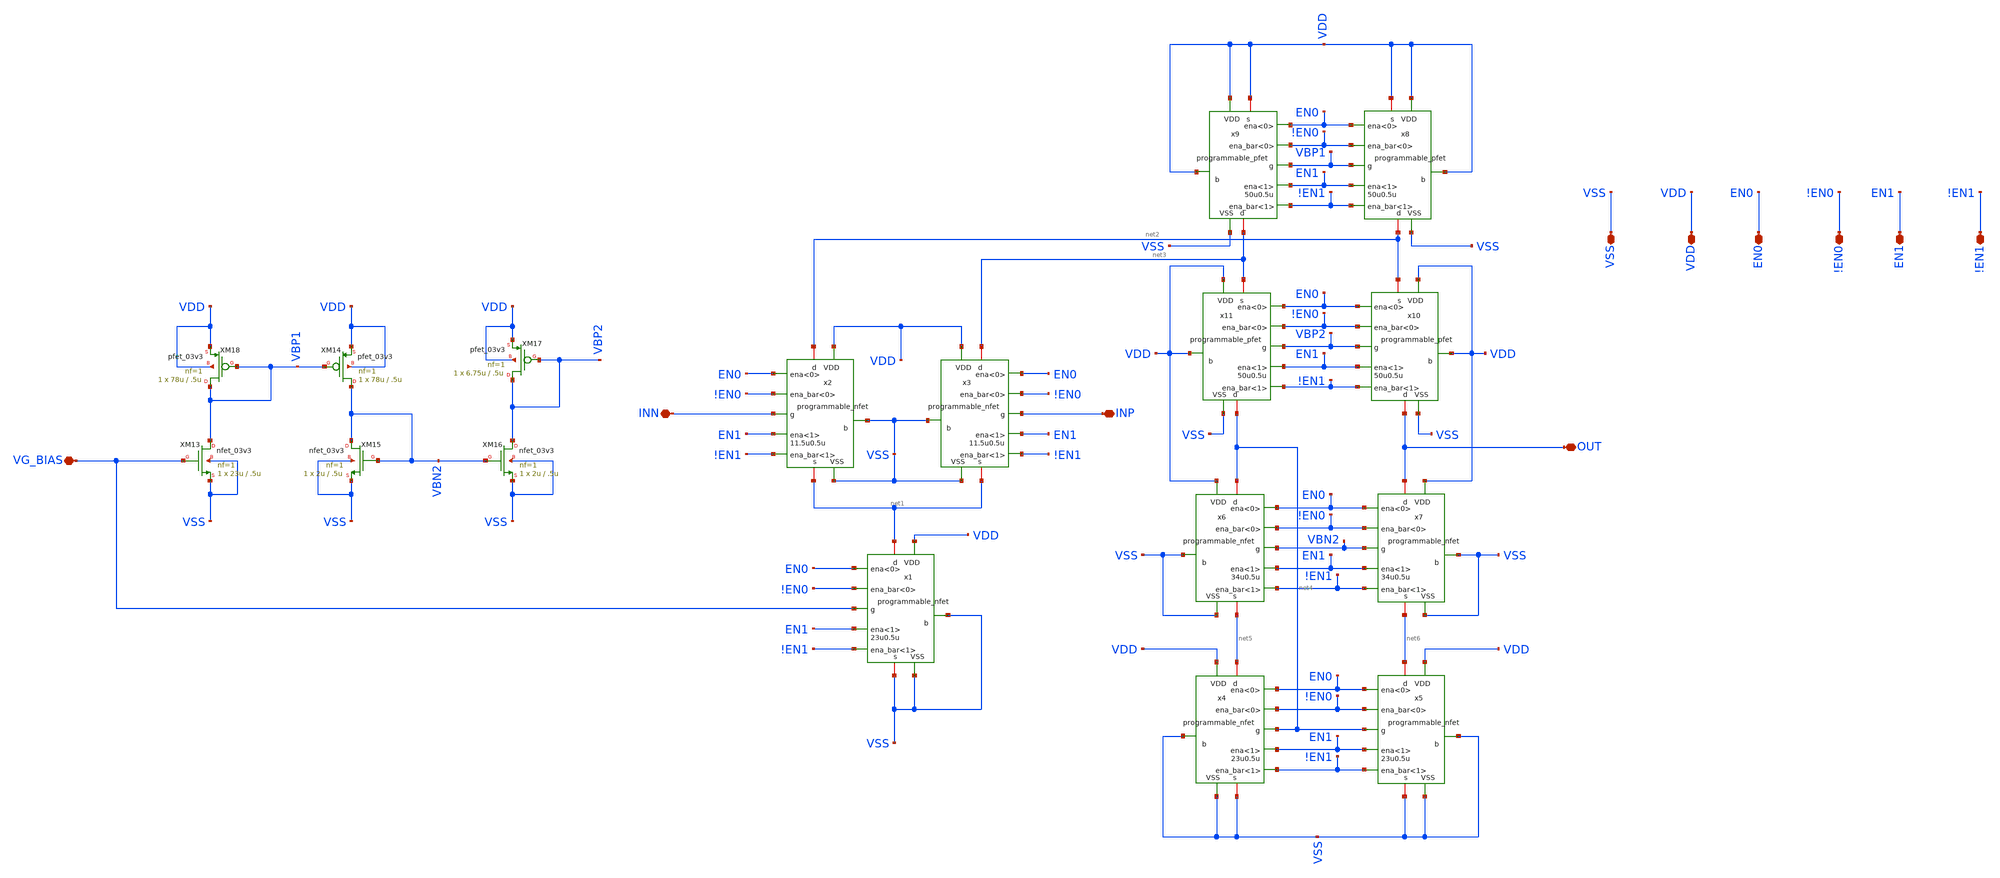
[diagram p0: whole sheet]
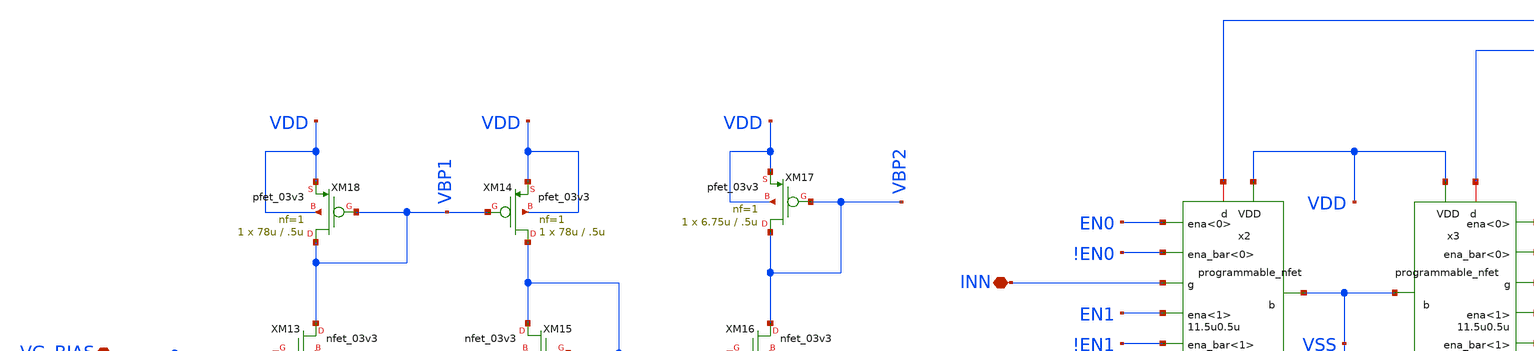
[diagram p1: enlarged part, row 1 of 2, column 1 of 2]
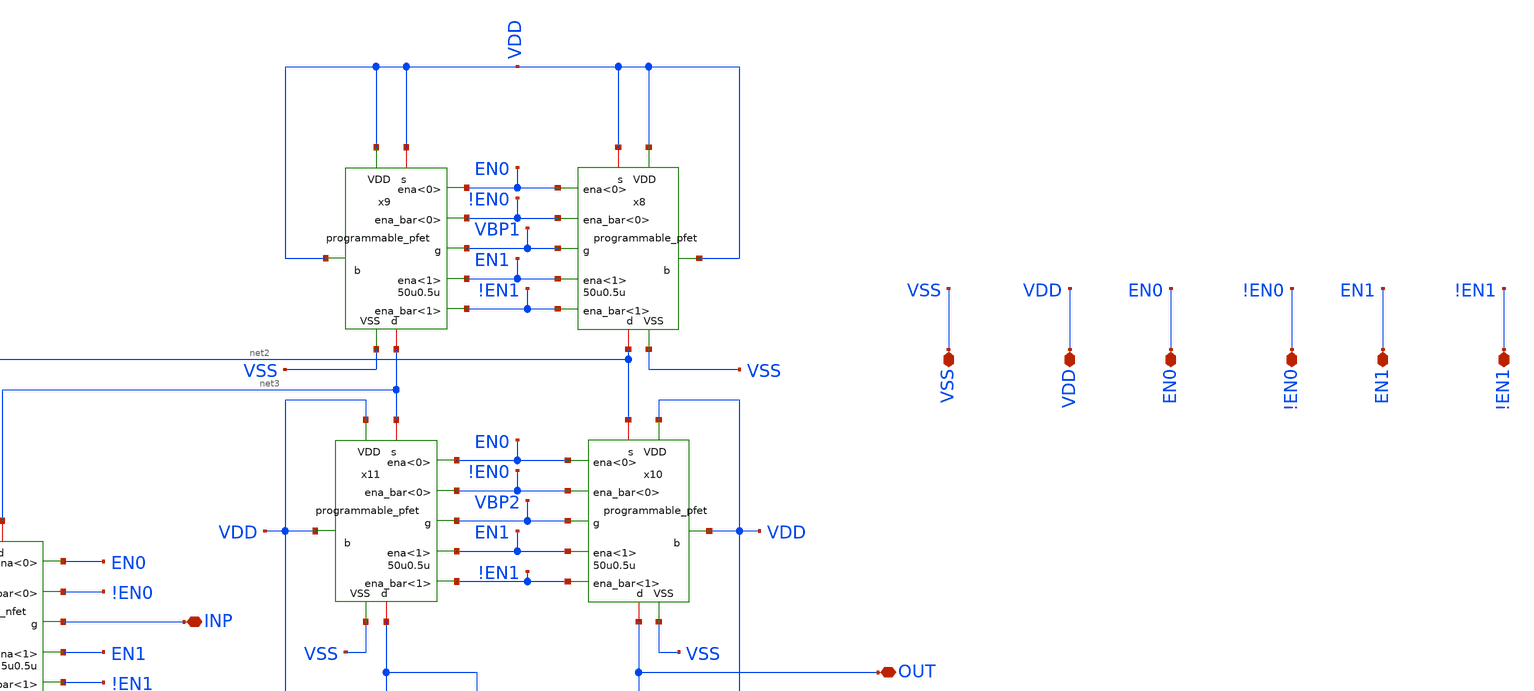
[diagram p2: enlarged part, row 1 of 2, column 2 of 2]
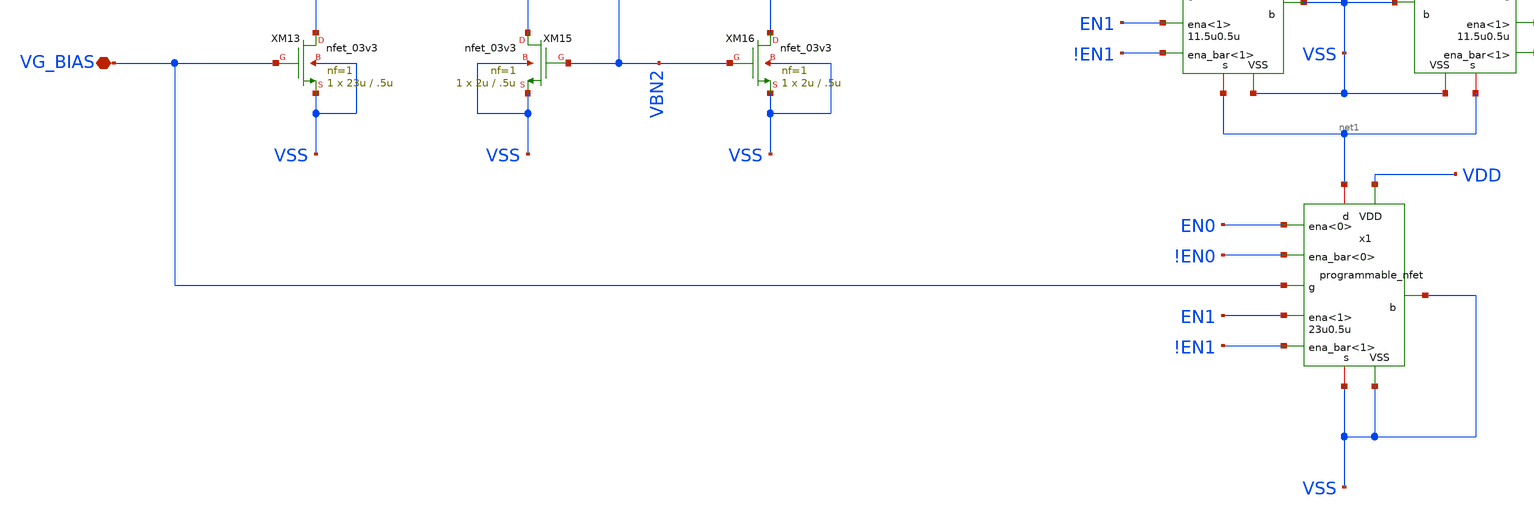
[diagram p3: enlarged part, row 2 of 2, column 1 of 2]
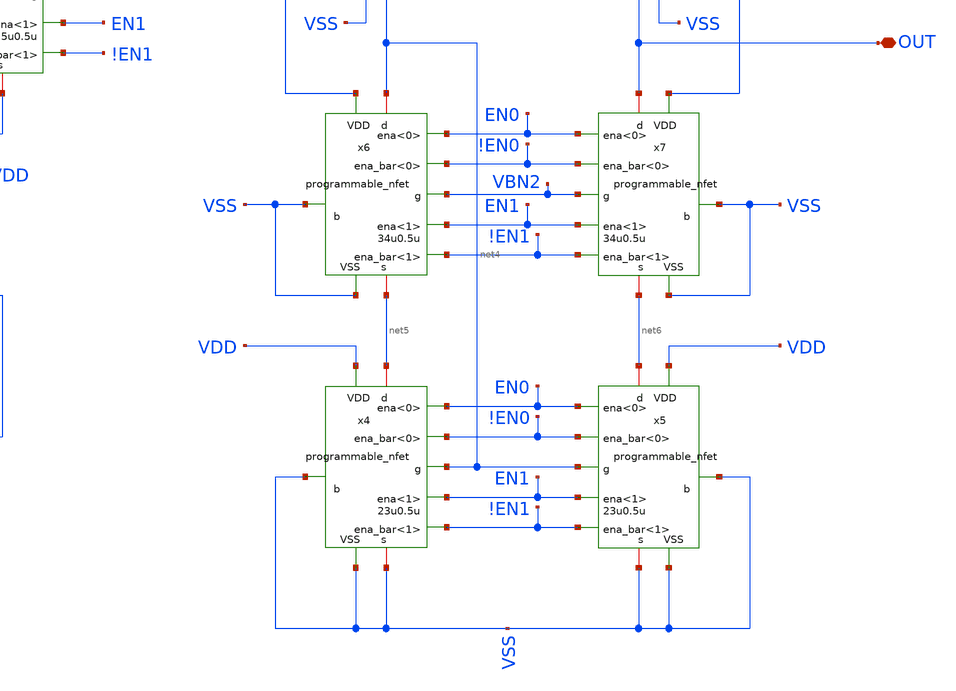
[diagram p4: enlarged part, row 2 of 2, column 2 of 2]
** sch_path: designs/libs/old_amps/ota_folded_cascode/programmable_folded.sch
**.subckt programmable_folded OUT VSS VDD EN0 !EN0 EN1 !EN1 INN INP VG_BIAS
*.iopin OUT
*.iopin VSS
*.iopin VDD
*.iopin EN0
*.iopin !EN0
*.iopin EN1
*.iopin !EN1
*.iopin INN
*.iopin INP
*.iopin VG_BIAS
XM18 VBP1 VBP1 VDD VDD pfet_03v3 L=.5u W=78u nf=1 ad='int((nf+1)/2) * W/nf * 0.18u' as='int((nf+2)/2) * W/nf * 0.18u'
+ pd='2*int((nf+1)/2) * (W/nf + 0.18u)' ps='2*int((nf+2)/2) * (W/nf + 0.18u)' nrd='0.18u / W' nrs='0.18u / W'
+ sa=0 sb=0 sd=0 m=1
XM13 VBP1 VG_BIAS VSS VSS nfet_03v3 L=.5u W=23u nf=1 ad='int((nf+1)/2) * W/nf * 0.18u' as='int((nf+2)/2) * W/nf * 0.18u'
+ pd='2*int((nf+1)/2) * (W/nf + 0.18u)' ps='2*int((nf+2)/2) * (W/nf + 0.18u)' nrd='0.18u / W' nrs='0.18u / W'
+ sa=0 sb=0 sd=0 m=1
XM14 VBN2 VBP1 VDD VDD pfet_03v3 L=.5u W=78u nf=1 ad='int((nf+1)/2) * W/nf * 0.18u' as='int((nf+2)/2) * W/nf * 0.18u'
+ pd='2*int((nf+1)/2) * (W/nf + 0.18u)' ps='2*int((nf+2)/2) * (W/nf + 0.18u)' nrd='0.18u / W' nrs='0.18u / W'
+ sa=0 sb=0 sd=0 m=1
XM15 VBN2 VBN2 VSS VSS nfet_03v3 L=.5u W=2u nf=1 ad='int((nf+1)/2) * W/nf * 0.18u' as='int((nf+2)/2) * W/nf * 0.18u'
+ pd='2*int((nf+1)/2) * (W/nf + 0.18u)' ps='2*int((nf+2)/2) * (W/nf + 0.18u)' nrd='0.18u / W' nrs='0.18u / W'
+ sa=0 sb=0 sd=0 m=1
XM16 VBP2 VBN2 VSS VSS nfet_03v3 L=.5u W=2u nf=1 ad='int((nf+1)/2) * W/nf * 0.18u' as='int((nf+2)/2) * W/nf * 0.18u'
+ pd='2*int((nf+1)/2) * (W/nf + 0.18u)' ps='2*int((nf+2)/2) * (W/nf + 0.18u)' nrd='0.18u / W' nrs='0.18u / W'
+ sa=0 sb=0 sd=0 m=1
XM17 VBP2 VBP2 VDD VDD pfet_03v3 L=.5u W=6.75u nf=1 ad='int((nf+1)/2) * W/nf * 0.18u' as='int((nf+2)/2) * W/nf * 0.18u'
+ pd='2*int((nf+1)/2) * (W/nf + 0.18u)' ps='2*int((nf+2)/2) * (W/nf + 0.18u)' nrd='0.18u / W' nrs='0.18u / W'
+ sa=0 sb=0 sd=0 m=1
x1 net1 VSS VG_BIAS VSS !EN0 VDD !EN1 EN0 EN1 VSS programmable_nfet width=23u length=0.5u
x2 net2 VSS INN net1 !EN0 VDD !EN1 EN0 EN1 VSS programmable_nfet width=11.5u length=0.5u
x3 net3 VSS INP net1 !EN0 VDD !EN1 EN0 EN1 VSS programmable_nfet width=11.5u length=0.5u
x4 net5 VSS net4 VSS !EN0 VDD !EN1 EN0 EN1 VSS programmable_nfet width=23u length=0.5u
x5 net6 VSS net4 VSS !EN0 VDD !EN1 EN0 EN1 VSS programmable_nfet width=23u length=0.5u
x6 net4 VSS VBN2 net5 !EN0 VDD !EN1 EN0 EN1 VSS programmable_nfet width=34u length=0.5u
x7 OUT VSS VBN2 net6 !EN0 VDD !EN1 EN0 EN1 VSS programmable_nfet width=34u length=0.5u
x8 net2 VDD VBP1 VDD !EN0 VDD !EN1 EN0 EN1 VSS programmable_pfet width=50u length=0.5u
x10 OUT VDD VBP2 net2 !EN0 VDD !EN1 EN0 EN1 VSS programmable_pfet width=50u length=0.5u
x11 net4 VDD VBP2 net3 !EN0 VDD !EN1 EN0 EN1 VSS programmable_pfet width=50u length=0.5u
x9 net3 VDD VBP1 VDD !EN0 VDD !EN1 EN0 EN1 VSS programmable_pfet width=50u length=0.5u
**.ends
.end
